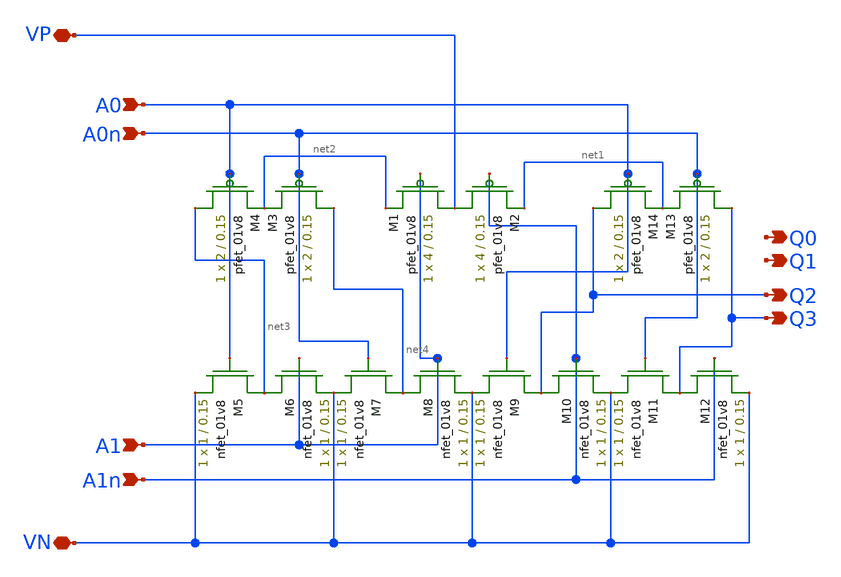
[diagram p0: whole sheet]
** sch_path: DRAM_Components/Schematic/PreDecode.sch
**.subckt PreDecode A0 A0n A1 A1n Q0 Q1 Q2 Q3 VP VN
*.ipin A0
*.ipin A0n
*.ipin A1
*.ipin A1n
*.opin Q0
*.opin Q1
*.opin Q2
*.opin Q3
*.iopin VP
*.iopin VN
XM2 VP A1n net1 VP sky130_fd_pr__pfet_01v8 L=0.15 W=4 nf=1 ad='int((nf+1)/2) * W/nf * 0.29' as='int((nf+2)/2) * W/nf * 0.29'
+ pd='2*int((nf+1)/2) * (W/nf + 0.29)' ps='2*int((nf+2)/2) * (W/nf + 0.29)' nrd='0.29 / W' nrs='0.29 / W'
+ sa=0 sb=0 sd=0 mult=1 m=1
XM1 VP A1 net2 VP sky130_fd_pr__pfet_01v8 L=0.15 W=4 nf=1 ad='int((nf+1)/2) * W/nf * 0.29' as='int((nf+2)/2) * W/nf * 0.29'
+ pd='2*int((nf+1)/2) * (W/nf + 0.29)' ps='2*int((nf+2)/2) * (W/nf + 0.29)' nrd='0.29 / W' nrs='0.29 / W'
+ sa=0 sb=0 sd=0 mult=1 m=1
XM5 net3 A0 VN VN sky130_fd_pr__nfet_01v8 L=0.15 W=1 nf=1 ad='int((nf+1)/2) * W/nf * 0.29' as='int((nf+2)/2) * W/nf * 0.29'
+ pd='2*int((nf+1)/2) * (W/nf + 0.29)' ps='2*int((nf+2)/2) * (W/nf + 0.29)' nrd='0.29 / W' nrs='0.29 / W'
+ sa=0 sb=0 sd=0 mult=1 m=1
XM3 net4 A0n net2 VP sky130_fd_pr__pfet_01v8 L=0.15 W=2 nf=1 ad='int((nf+1)/2) * W/nf * 0.29' as='int((nf+2)/2) * W/nf * 0.29'
+ pd='2*int((nf+1)/2) * (W/nf + 0.29)' ps='2*int((nf+2)/2) * (W/nf + 0.29)' nrd='0.29 / W' nrs='0.29 / W'
+ sa=0 sb=0 sd=0 mult=1 m=1
XM4 net3 A0 net2 VP sky130_fd_pr__pfet_01v8 L=0.15 W=2 nf=1 ad='int((nf+1)/2) * W/nf * 0.29' as='int((nf+2)/2) * W/nf * 0.29'
+ pd='2*int((nf+1)/2) * (W/nf + 0.29)' ps='2*int((nf+2)/2) * (W/nf + 0.29)' nrd='0.29 / W' nrs='0.29 / W'
+ sa=0 sb=0 sd=0 mult=1 m=1
XM6 net3 A1 VN VN sky130_fd_pr__nfet_01v8 L=0.15 W=1 nf=1 ad='int((nf+1)/2) * W/nf * 0.29' as='int((nf+2)/2) * W/nf * 0.29'
+ pd='2*int((nf+1)/2) * (W/nf + 0.29)' ps='2*int((nf+2)/2) * (W/nf + 0.29)' nrd='0.29 / W' nrs='0.29 / W'
+ sa=0 sb=0 sd=0 mult=1 m=1
XM7 net4 A0n VN VN sky130_fd_pr__nfet_01v8 L=0.15 W=1 nf=1 ad='int((nf+1)/2) * W/nf * 0.29' as='int((nf+2)/2) * W/nf * 0.29'
+ pd='2*int((nf+1)/2) * (W/nf + 0.29)' ps='2*int((nf+2)/2) * (W/nf + 0.29)' nrd='0.29 / W' nrs='0.29 / W'
+ sa=0 sb=0 sd=0 mult=1 m=1
XM8 net4 A1 VN VN sky130_fd_pr__nfet_01v8 L=0.15 W=1 nf=1 ad='int((nf+1)/2) * W/nf * 0.29' as='int((nf+2)/2) * W/nf * 0.29'
+ pd='2*int((nf+1)/2) * (W/nf + 0.29)' ps='2*int((nf+2)/2) * (W/nf + 0.29)' nrd='0.29 / W' nrs='0.29 / W'
+ sa=0 sb=0 sd=0 mult=1 m=1
XM9 Q2 A0 VN VN sky130_fd_pr__nfet_01v8 L=0.15 W=1 nf=1 ad='int((nf+1)/2) * W/nf * 0.29' as='int((nf+2)/2) * W/nf * 0.29'
+ pd='2*int((nf+1)/2) * (W/nf + 0.29)' ps='2*int((nf+2)/2) * (W/nf + 0.29)' nrd='0.29 / W' nrs='0.29 / W'
+ sa=0 sb=0 sd=0 mult=1 m=1
XM10 Q2 A1n VN VN sky130_fd_pr__nfet_01v8 L=0.15 W=1 nf=1 ad='int((nf+1)/2) * W/nf * 0.29' as='int((nf+2)/2) * W/nf * 0.29'
+ pd='2*int((nf+1)/2) * (W/nf + 0.29)' ps='2*int((nf+2)/2) * (W/nf + 0.29)' nrd='0.29 / W' nrs='0.29 / W'
+ sa=0 sb=0 sd=0 mult=1 m=1
XM11 Q3 A0n VN VN sky130_fd_pr__nfet_01v8 L=0.15 W=1 nf=1 ad='int((nf+1)/2) * W/nf * 0.29' as='int((nf+2)/2) * W/nf * 0.29'
+ pd='2*int((nf+1)/2) * (W/nf + 0.29)' ps='2*int((nf+2)/2) * (W/nf + 0.29)' nrd='0.29 / W' nrs='0.29 / W'
+ sa=0 sb=0 sd=0 mult=1 m=1
XM12 Q3 A1n VN VN sky130_fd_pr__nfet_01v8 L=0.15 W=1 nf=1 ad='int((nf+1)/2) * W/nf * 0.29' as='int((nf+2)/2) * W/nf * 0.29'
+ pd='2*int((nf+1)/2) * (W/nf + 0.29)' ps='2*int((nf+2)/2) * (W/nf + 0.29)' nrd='0.29 / W' nrs='0.29 / W'
+ sa=0 sb=0 sd=0 mult=1 m=1
XM13 Q3 A0n net1 VP sky130_fd_pr__pfet_01v8 L=0.15 W=2 nf=1 ad='int((nf+1)/2) * W/nf * 0.29' as='int((nf+2)/2) * W/nf * 0.29'
+ pd='2*int((nf+1)/2) * (W/nf + 0.29)' ps='2*int((nf+2)/2) * (W/nf + 0.29)' nrd='0.29 / W' nrs='0.29 / W'
+ sa=0 sb=0 sd=0 mult=1 m=1
XM14 Q2 A0 net1 VP sky130_fd_pr__pfet_01v8 L=0.15 W=2 nf=1 ad='int((nf+1)/2) * W/nf * 0.29' as='int((nf+2)/2) * W/nf * 0.29'
+ pd='2*int((nf+1)/2) * (W/nf + 0.29)' ps='2*int((nf+2)/2) * (W/nf + 0.29)' nrd='0.29 / W' nrs='0.29 / W'
+ sa=0 sb=0 sd=0 mult=1 m=1
**.ends
.end
